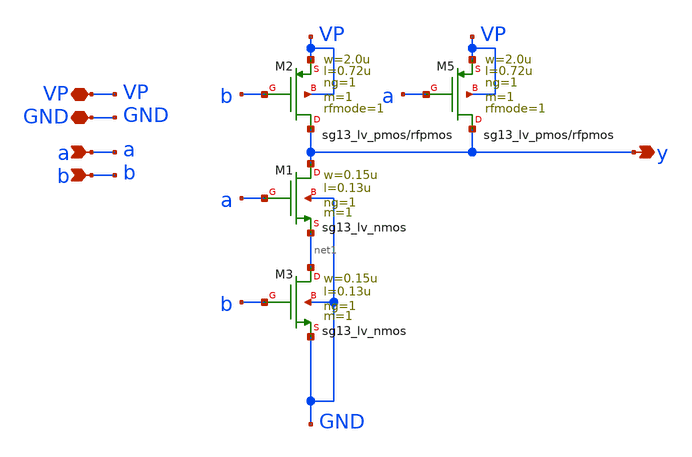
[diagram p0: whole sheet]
** sch_path: schematics/divider/NAND_2in.sch
**.subckt NAND_2in y GND a VP b
*.opin y
*.iopin GND
*.ipin a
*.iopin VP
*.ipin b
XM1 y a net1 GND sg13_lv_nmos w=0.15u l=0.13u ng=1 m=1 mm_ok=1
XM2 y b VP VP sg13_lv_pmos w=2.0u l=0.72u ng=1 m=1 rfmode=1 mm_ok=1
XM3 net1 b GND GND sg13_lv_nmos w=0.15u l=0.13u ng=1 m=1 mm_ok=1
XM5 y a VP VP sg13_lv_pmos w=2.0u l=0.72u ng=1 m=1 rfmode=1 mm_ok=1
**.ends
.end
